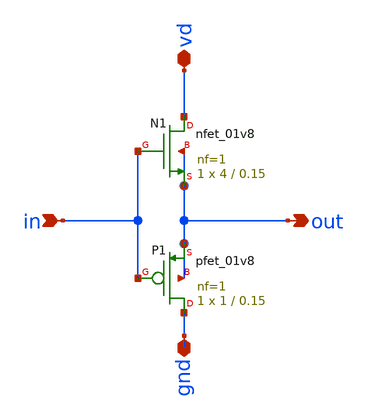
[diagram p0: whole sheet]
** sch_path: mag/sigma-delta_modulator/xschem/comp.sch
* Copyright 2020 Stefan Frederik Schippers
* Licensed under the Apache License, Version 2.0 (the "License");
* you may not use this file except in compliance with the License.
* You may obtain a copy of the License at
* https://www.apache.org/licenses/LICENSE-2.0
* Unless required by applicable law or agreed to in writing, software
* distributed under the License is distributed on an "AS IS" BASIS,
* WITHOUT WARRANTIES OR CONDITIONS OF ANY KIND, either express or implied.
* See the License for the specific language governing permissions and
* limitations under the License.
**.subckt comp in gnd out vd
*.ipin in
*.iopin gnd
*.opin out
*.iopin vd
XN1 vd in out out sky130_fd_pr__nfet_01v8 L=0.15 W=4 nf=1 ad='int((nf+1)/2) * W/nf * 0.29' as='int((nf+2)/2) * W/nf * 0.29'
+ pd='2*int((nf+1)/2) * (W/nf + 0.29)' ps='2*int((nf+2)/2) * (W/nf + 0.29)' nrd='0.29 / W' nrs='0.29 / W'
+ sa=0 sb=0 sd=0 mult=1 m=1
XP1 gnd in out out sky130_fd_pr__pfet_01v8 L=0.15 W=1 nf=1 ad='int((nf+1)/2) * W/nf * 0.29' as='int((nf+2)/2) * W/nf * 0.29'
+ pd='2*int((nf+1)/2) * (W/nf + 0.29)' ps='2*int((nf+2)/2) * (W/nf + 0.29)' nrd='0.29 / W' nrs='0.29 / W'
+ sa=0 sb=0 sd=0 mult=1 m=1
**** begin user architecture code




**** end user architecture code
**.ends
.end
